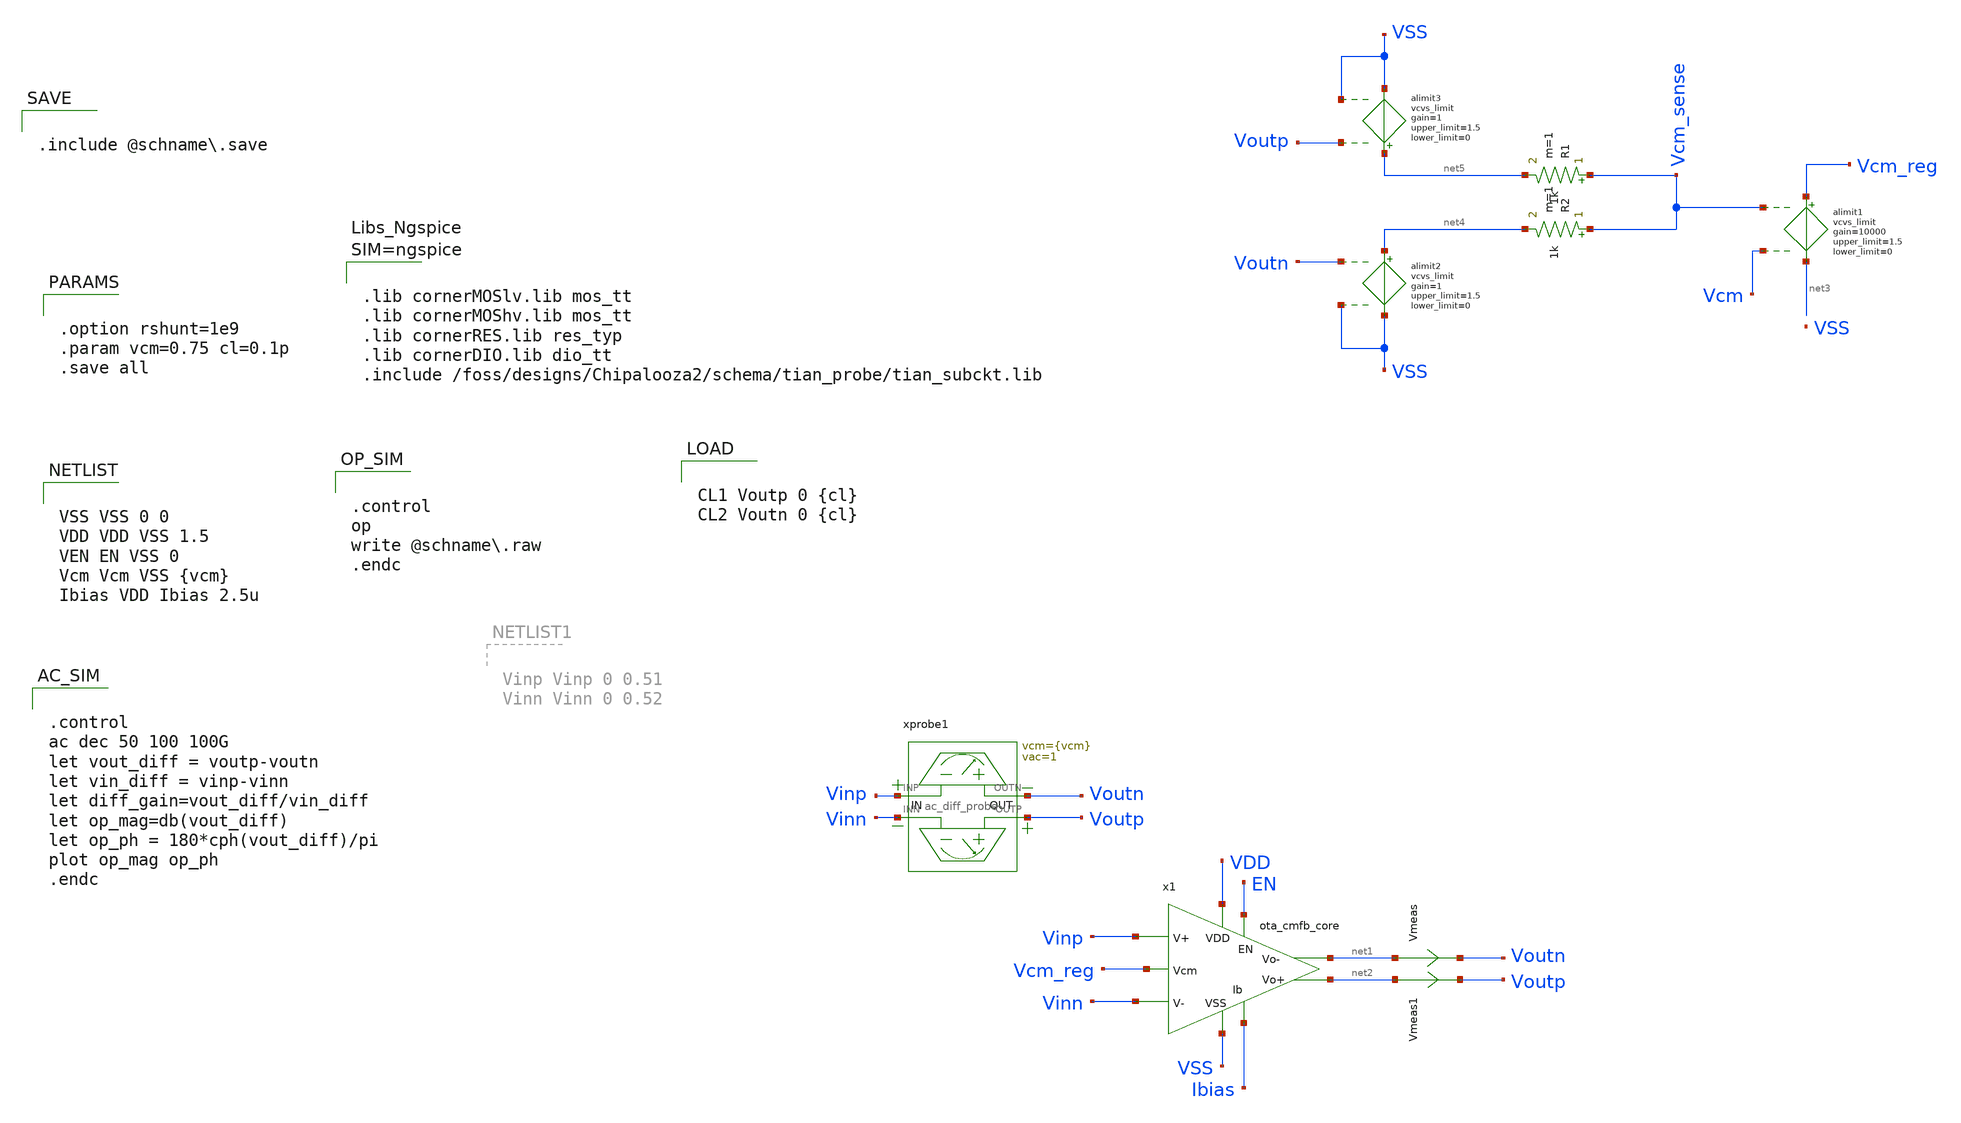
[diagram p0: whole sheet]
** sch_path: schema/ota_cmfb_core/ota_cmfb_core_tb.sch
**.subckt ota_cmfb_core_tb
x1 VDD Vcm_reg Vinn Vinp Ibias net1 net2 VSS EN ota_cmfb_core
alimit1 %vd( Vcm_sense Vcm ) %vd( Vcm_reg net3 ) alimit1
.model alimit1 limit ( gain=10000 out_lower_limit=0 out_upper_limit=1.5 )
xprobe1 Vinp Voutn Vinn Voutp ac_diff_probe vcm={vcm} vac=1
alimit2 %vd( Voutn VSS ) %vd( net4 VSS ) alimit2
.model alimit2 limit ( gain=1 out_lower_limit=0 out_upper_limit=1.5 )
alimit3 %vd( Voutp VSS ) %vd( net5 VSS ) alimit3
.model alimit3 limit ( gain=1 out_lower_limit=0 out_upper_limit=1.5 )
R1 Vcm_sense net5 1k m=1
R2 Vcm_sense net4 1k m=1
Vmeas net1 Voutn 0
.save i(vmeas)
Vmeas1 net2 Voutp 0
.save i(vmeas1)
**** begin user architecture code


VSS VSS 0 0
VDD VDD VSS 1.5
VEN EN VSS 0
Vcm Vcm VSS {vcm}
Ibias VDD Ibias 2.5u



.control
op
write @schname.raw
.endc




.lib cornerMOSlv.lib mos_tt
.lib cornerMOShv.lib mos_tt
.lib cornerRES.lib res_typ
.lib cornerDIO.lib dio_tt
.include /foss/designs/Chipalooza2/schema/tian_probe/tian_subckt.lib





.control
ac dec 50 100 100G
let vout_diff = voutp-voutn
let vin_diff = vinp-vinn
let diff_gain=vout_diff/vin_diff
let op_mag=db(vout_diff)
let op_ph = 180*cph(vout_diff)/pi
plot op_mag op_ph
.endc




.option rshunt=1e9
.param vcm=0.75 cl=0.1p
.save all




CL1 Voutp 0 {cl}
CL2 Voutn 0 {cl}



.include @schname.save

**** end user architecture code
**.ends

* expanding   symbol:  /foss/designs/Chipalooza2/schema/ota_cmfb_core/ota_cmfb_core.sym # of pins=9
** sym_path: schema/ota_cmfb_core/ota_cmfb_core.sym
** sch_path: schema/ota_cmfb_core/ota_cmfb_core.sch
.subckt ota_cmfb_core VDD Vcm_reg Vinn Vinp Ibias Voutn Voutp VSS EN
*.opin Voutn
*.opin Voutp
*.iopin VDD
*.iopin VSS
*.ipin Vinp
*.ipin Ibias
*.ipin Vinn
*.ipin Vcm_reg
*.ipin EN
XM1 Voutp Ibias VSS VSS sg13_lv_nmos w=0.5u l=10u ng=1 m=4 mm_ok=1
XM2 net1 Vinn Voutp VDD sg13_lv_pmos w=2.5u l=2u ng=1 m=8 mm_ok=1
XM3 Voutn Ibias VSS VSS sg13_lv_nmos w=0.5u l=10u ng=1 m=4 mm_ok=1
XM4 net1 Vinp Voutn VDD sg13_lv_pmos w=2.5u l=2u ng=1 m=8 mm_ok=1
XM5 VDD Vcm_reg net1 VDD sg13_lv_pmos w=2.5u l=5u ng=1 m=4 mm_ok=1
XM6 Ibias Ibias VSS VSS sg13_lv_nmos w=0.5u l=10u ng=1 m=1 mm_ok=1
XM7 Ibias EN VSS VSS sg13_lv_nmos w=0.15u l=0.13u ng=1 m=1 mm_ok=1
.ends


* expanding   symbol:  /foss/designs/Chipalooza2/schema/ac_diff_probe/ac_diff_probe.sym # of pins=4
** sym_path: schema/ac_diff_probe/ac_diff_probe.sym
** sch_path: schema/ac_diff_probe/ac_diff_probe.sch
.subckt ac_diff_probe INP OUTN INN OUTP  vcm=0.75 vac=0.1
*.iopin OUTN
*.iopin INP
*.iopin OUTP
*.iopin INN
xprobe1 OUTN INP ac_probe vcm={vcm} vac={vac}
xprobe2 OUTP INN ac_probe vcm={vcm} vac=-{vac}
.ends


* expanding   symbol:  /foss/designs/Chipalooza2/schema/ac_probe/ac_probe.sym # of pins=2
** sym_path: schema/ac_probe/ac_probe.sym
** sch_path: schema/ac_probe/ac_probe.sch
.subckt ac_probe OUT IN  vcm=0.75 vac=0.01

*.iopin IN
*.iopin OUT
C1 net1 IN 1 m=1
V1 net1 0 {vcm} ac {vac}
L1 OUT net2 1G m=1
R1 net2 IN 1m m=1
.ends

.end
